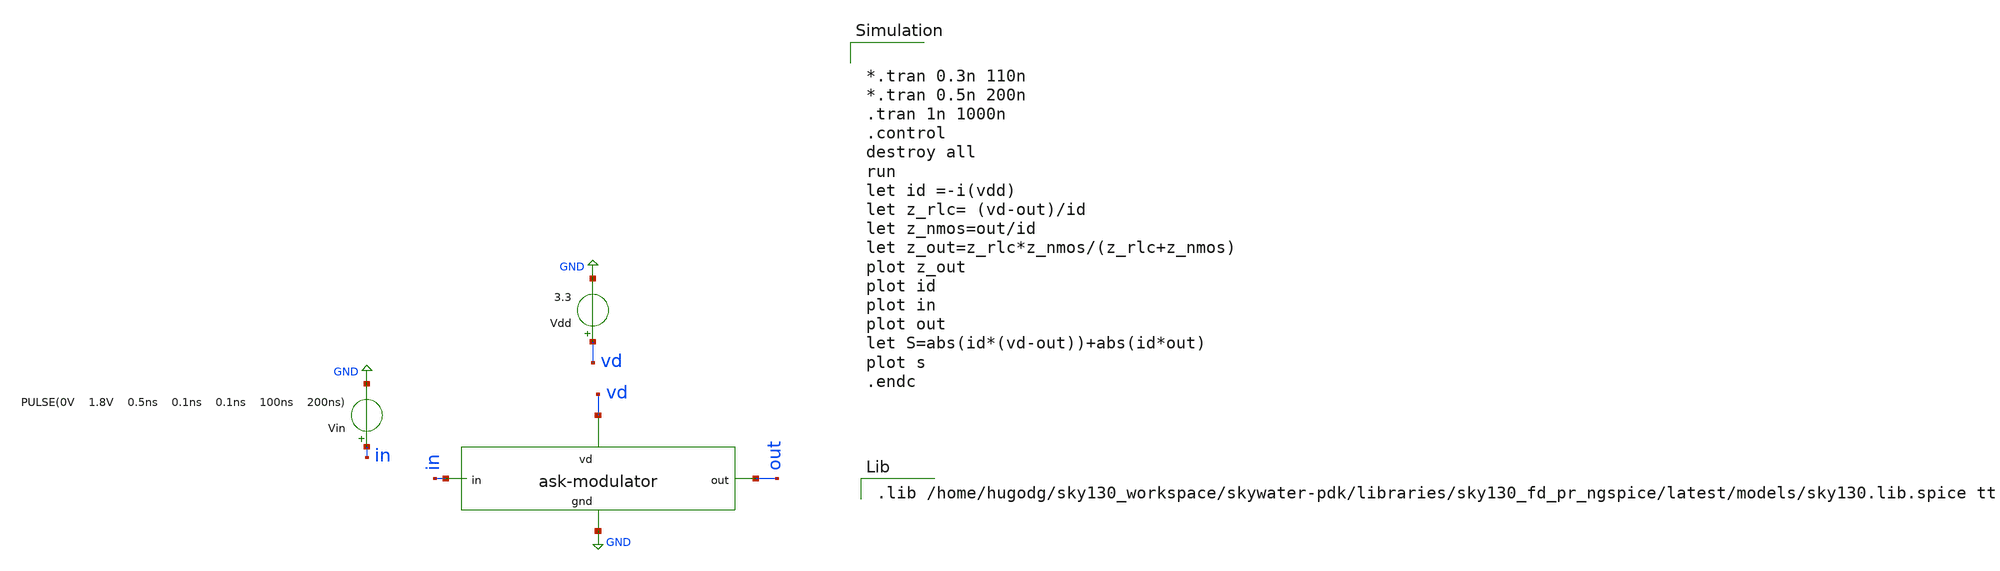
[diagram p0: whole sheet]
** sch_path: ask_modulator/xschem/ask-modulator_tb-tran.sch
**.subckt ask-modulator_tb-tran
Vdd vd GND 3.3
Vin in GND PULSE(0V 1.8V 0.5ns 0.1ns 0.1ns 100ns 200ns)
x1 vd out in GND ask-modulator
**** begin user architecture code


*.tran 0.3n 110n
*.tran 0.5n 200n
.tran 1n 1000n
.control
destroy all
run
let id =-i(vdd)
let z_rlc= (vd-out)/id
let z_nmos=out/id
let z_out=z_rlc*z_nmos/(z_rlc+z_nmos)
plot z_out
plot id
plot in
plot out
let S=abs(id*(vd-out))+abs(id*out)
plot s
.endc


.lib /home/hugodg/sky130_workspace/skywater-pdk/libraries/sky130_fd_pr_ngspice/latest/models/sky130.lib.spice tt

**** end user architecture code
**.ends
.GLOBAL GND
.end
